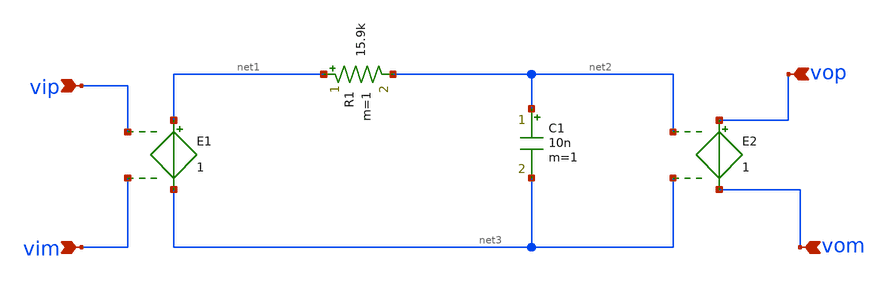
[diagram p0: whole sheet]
** sch_path: work/xschem/buffer.sch
**.subckt buffer vop vom vim vip
*.ipin vop
*.ipin vom
*.ipin vim
*.ipin vip
E1 net1 net3 vip vim 1
R1 net1 net2 15.9k m=1
C1 net2 net3 10n m=1
E2 vop vom net2 net3 1
**.ends
.end
